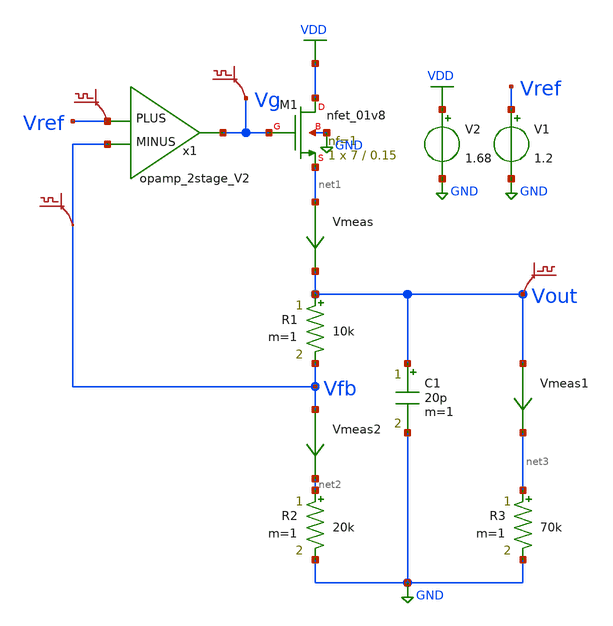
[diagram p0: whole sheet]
** sch_path: lib/xschem/LDO/LDO.sch
**.subckt LDO
V1 Vref GND 1.2
V2 VDD GND 1.68
R1 Vout Vfb 10k m=1
R2 net2 GND 20k m=1
C1 Vout GND 20p m=1
R3 net3 GND 70k m=1
x1 Vfb Vref Vg VDD GND opamp_2stage_V2
.save v(vref)
.save v(vout)
Vmeas net1 Vout 0
.save i(vmeas)
.save v(vg)
XM1 VDD Vg net1 GND sky130_fd_pr__nfet_01v8 L=0.15 W=7 nf=1 ad='int((nf+1)/2) * W/nf * 0.29' as='int((nf+2)/2) * W/nf * 0.29'
+ pd='2*int((nf+1)/2) * (W/nf + 0.29)' ps='2*int((nf+2)/2) * (W/nf + 0.29)' nrd='0.29 / W' nrs='0.29 / W'
+ sa=0 sb=0 sd=0 mult=1 m=1
.save v(vfb)
Vmeas1 Vout net3 0
.save i(vmeas1)
Vmeas2 Vfb net2 0
.save i(vmeas2)
**** begin user architecture code

.lib $::SKYWATER_MODELS/sky130.lib.spice tt


**** end user architecture code
**.ends

* expanding   symbol:  LDO/opamp_2stage_V2.sym # of pins=3
** sym_path: lib/xschem/LDO/opamp_2stage_V2.sym
** sch_path: lib/xschem/LDO/opamp_2stage_V2.sch
.subckt opamp_2stage_V2 MINUS PLUS Vout VDD GND
*.ipin PLUS
*.ipin MINUS
*.opin Vout
C3 net6 Vout 2p m=1
XM6 net3 net3 GND GND sky130_fd_pr__nfet_01v8 L=0.15 W=2 nf=1 ad='int((nf+1)/2) * W/nf * 0.29' as='int((nf+2)/2) * W/nf * 0.29'
+ pd='2*int((nf+1)/2) * (W/nf + 0.29)' ps='2*int((nf+2)/2) * (W/nf + 0.29)' nrd='0.29 / W' nrs='0.29 / W'
+ sa=0 sb=0 sd=0 mult=1 m=1
XM5 net5 net3 GND GND sky130_fd_pr__nfet_01v8 L=0.15 W=2 nf=1 ad='int((nf+1)/2) * W/nf * 0.29' as='int((nf+2)/2) * W/nf * 0.29'
+ pd='2*int((nf+1)/2) * (W/nf + 0.29)' ps='2*int((nf+2)/2) * (W/nf + 0.29)' nrd='0.29 / W' nrs='0.29 / W'
+ sa=0 sb=0 sd=0 mult=1 m=1
XM7 net2 PLUS net1 VDD sky130_fd_pr__pfet_01v8 L=0.15 W=5 nf=1 ad='int((nf+1)/2) * W/nf * 0.29' as='int((nf+2)/2) * W/nf * 0.29'
+ pd='2*int((nf+1)/2) * (W/nf + 0.29)' ps='2*int((nf+2)/2) * (W/nf + 0.29)' nrd='0.29 / W' nrs='0.29 / W'
+ sa=0 sb=0 sd=0 mult=1 m=1
XM10 net4 MINUS net1 VDD sky130_fd_pr__pfet_01v8 L=0.15 W=5 nf=1 ad='int((nf+1)/2) * W/nf * 0.29' as='int((nf+2)/2) * W/nf * 0.29'
+ pd='2*int((nf+1)/2) * (W/nf + 0.29)' ps='2*int((nf+2)/2) * (W/nf + 0.29)' nrd='0.29 / W' nrs='0.29 / W'
+ sa=0 sb=0 sd=0 mult=1 m=1
XM11 net1 Vbias VDD VDD sky130_fd_pr__pfet_01v8 L=0.15 W=5 nf=1 ad='int((nf+1)/2) * W/nf * 0.29' as='int((nf+2)/2) * W/nf * 0.29'
+ pd='2*int((nf+1)/2) * (W/nf + 0.29)' ps='2*int((nf+2)/2) * (W/nf + 0.29)' nrd='0.29 / W' nrs='0.29 / W'
+ sa=0 sb=0 sd=0 mult=1 m=1
XM13 Vout net5 GND GND sky130_fd_pr__nfet_01v8 L=0.15 W=5 nf=1 ad='int((nf+1)/2) * W/nf * 0.29' as='int((nf+2)/2) * W/nf * 0.29'
+ pd='2*int((nf+1)/2) * (W/nf + 0.29)' ps='2*int((nf+2)/2) * (W/nf + 0.29)' nrd='0.29 / W' nrs='0.29 / W'
+ sa=0 sb=0 sd=0 mult=1 m=1
XM16 net7 Vbias VDD VDD sky130_fd_pr__pfet_01v8 L=0.15 W=5 nf=1 ad='int((nf+1)/2) * W/nf * 0.29' as='int((nf+2)/2) * W/nf * 0.29'
+ pd='2*int((nf+1)/2) * (W/nf + 0.29)' ps='2*int((nf+2)/2) * (W/nf + 0.29)' nrd='0.29 / W' nrs='0.29 / W'
+ sa=0 sb=0 sd=0 mult=1 m=1
.save v(plus)
.save v(minus)
.save v(net2)
.save v(net4)
.save v(minus)
.save v(vout)
.save v(plus)
Vmeas1 net4 net3 0
.save i(vmeas1)
Vmeas2 net2 net5 0
.save i(vmeas2)
Vmeas3 net7 Vout 0
.save i(vmeas3)
Vmeas5 net2 net8 0
.save i(vmeas5)
x1 Vbias Vcs VDD GND casc_mirror
XM1 net6 Vcs net8 GND sky130_fd_pr__nfet_01v8 L=0.15 W=1 nf=1 ad='int((nf+1)/2) * W/nf * 0.29' as='int((nf+2)/2) * W/nf * 0.29'
+ pd='2*int((nf+1)/2) * (W/nf + 0.29)' ps='2*int((nf+2)/2) * (W/nf + 0.29)' nrd='0.29 / W' nrs='0.29 / W'
+ sa=0 sb=0 sd=0 mult=1 m=1
.save v(net6)
.save v(vbias)
.save v(vbias)
.ends


* expanding   symbol:  LDO/casc_mirror.sym # of pins=2
** sym_path: lib/xschem/LDO/casc_mirror.sym
** sch_path: lib/xschem/LDO/casc_mirror.sch
.subckt casc_mirror Vbias Vcs VDD GND
*.opin Vbias
*.opin Vcs
XM8 Vbias Vbias net3 VDD sky130_fd_pr__pfet_01v8 L=0.15 W=2 nf=1 ad='int((nf+1)/2) * W/nf * 0.29' as='int((nf+2)/2) * W/nf * 0.29'
+ pd='2*int((nf+1)/2) * (W/nf + 0.29)' ps='2*int((nf+2)/2) * (W/nf + 0.29)' nrd='0.29 / W' nrs='0.29 / W'
+ sa=0 sb=0 sd=0 mult=1 m=1
XM9 net7 net1 net4 GND sky130_fd_pr__nfet_01v8 L=0.15 W=7 nf=1 ad='int((nf+1)/2) * W/nf * 0.29' as='int((nf+2)/2) * W/nf * 0.29'
+ pd='2*int((nf+1)/2) * (W/nf + 0.29)' ps='2*int((nf+2)/2) * (W/nf + 0.29)' nrd='0.29 / W' nrs='0.29 / W'
+ sa=0 sb=0 sd=0 mult=1 m=1
XM1 Vcs Vbias net3 VDD sky130_fd_pr__pfet_01v8 L=0.15 W=2 nf=1 ad='int((nf+1)/2) * W/nf * 0.29' as='int((nf+2)/2) * W/nf * 0.29'
+ pd='2*int((nf+1)/2) * (W/nf + 0.29)' ps='2*int((nf+2)/2) * (W/nf + 0.29)' nrd='0.29 / W' nrs='0.29 / W'
+ sa=0 sb=0 sd=0 mult=1 m=1
XM2 net9 net2 net8 GND sky130_fd_pr__nfet_01v8 L=0.15 W=2 nf=1 ad='int((nf+1)/2) * W/nf * 0.29' as='int((nf+2)/2) * W/nf * 0.29'
+ pd='2*int((nf+1)/2) * (W/nf + 0.29)' ps='2*int((nf+2)/2) * (W/nf + 0.29)' nrd='0.29 / W' nrs='0.29 / W'
+ sa=0 sb=0 sd=0 mult=1 m=1
XM3 net2 net2 net6 GND sky130_fd_pr__nfet_01v8 L=0.15 W=2 nf=1 ad='int((nf+1)/2) * W/nf * 0.29' as='int((nf+2)/2) * W/nf * 0.29'
+ pd='2*int((nf+1)/2) * (W/nf + 0.29)' ps='2*int((nf+2)/2) * (W/nf + 0.29)' nrd='0.29 / W' nrs='0.29 / W'
+ sa=0 sb=0 sd=0 mult=1 m=1
XM4 net1 net1 GND GND sky130_fd_pr__nfet_01v8 L=0.15 W=2 nf=1 ad='int((nf+1)/2) * W/nf * 0.29' as='int((nf+2)/2) * W/nf * 0.29'
+ pd='2*int((nf+1)/2) * (W/nf + 0.29)' ps='2*int((nf+2)/2) * (W/nf + 0.29)' nrd='0.29 / W' nrs='0.29 / W'
+ sa=0 sb=0 sd=0 mult=1 m=1
R1 net5 GND 1k m=1
Vmeas_ref2 net4 net5 0
.save i(vmeas_ref2)
Vmeas1 net6 net1 0
.save i(vmeas1)
Vmeas_ref1 net8 net7 0
.save i(vmeas_ref1)
.save v(net7)
.save v(net5)
.save v(net1)
Vmeas_ref3 Vbias net9 0
.save i(vmeas_ref3)
Vmeas_ref4 Vcs net2 0
.save i(vmeas_ref4)
Vmeas_ref5 VDD net10 0
.save i(vmeas_ref5)
I0 net10 net3 0.25u
.save v(vbias)
.save v(vcs)
.ends

.GLOBAL VDD
.GLOBAL GND
**** begin user architecture code



.control
save all
op
write LDO.raw
*dc V2 1.62 1.98 0.005
*plot v(Vout) v(Vfb) v(Vg) vs v(VDD)
.endc


**** end user architecture code
.end
